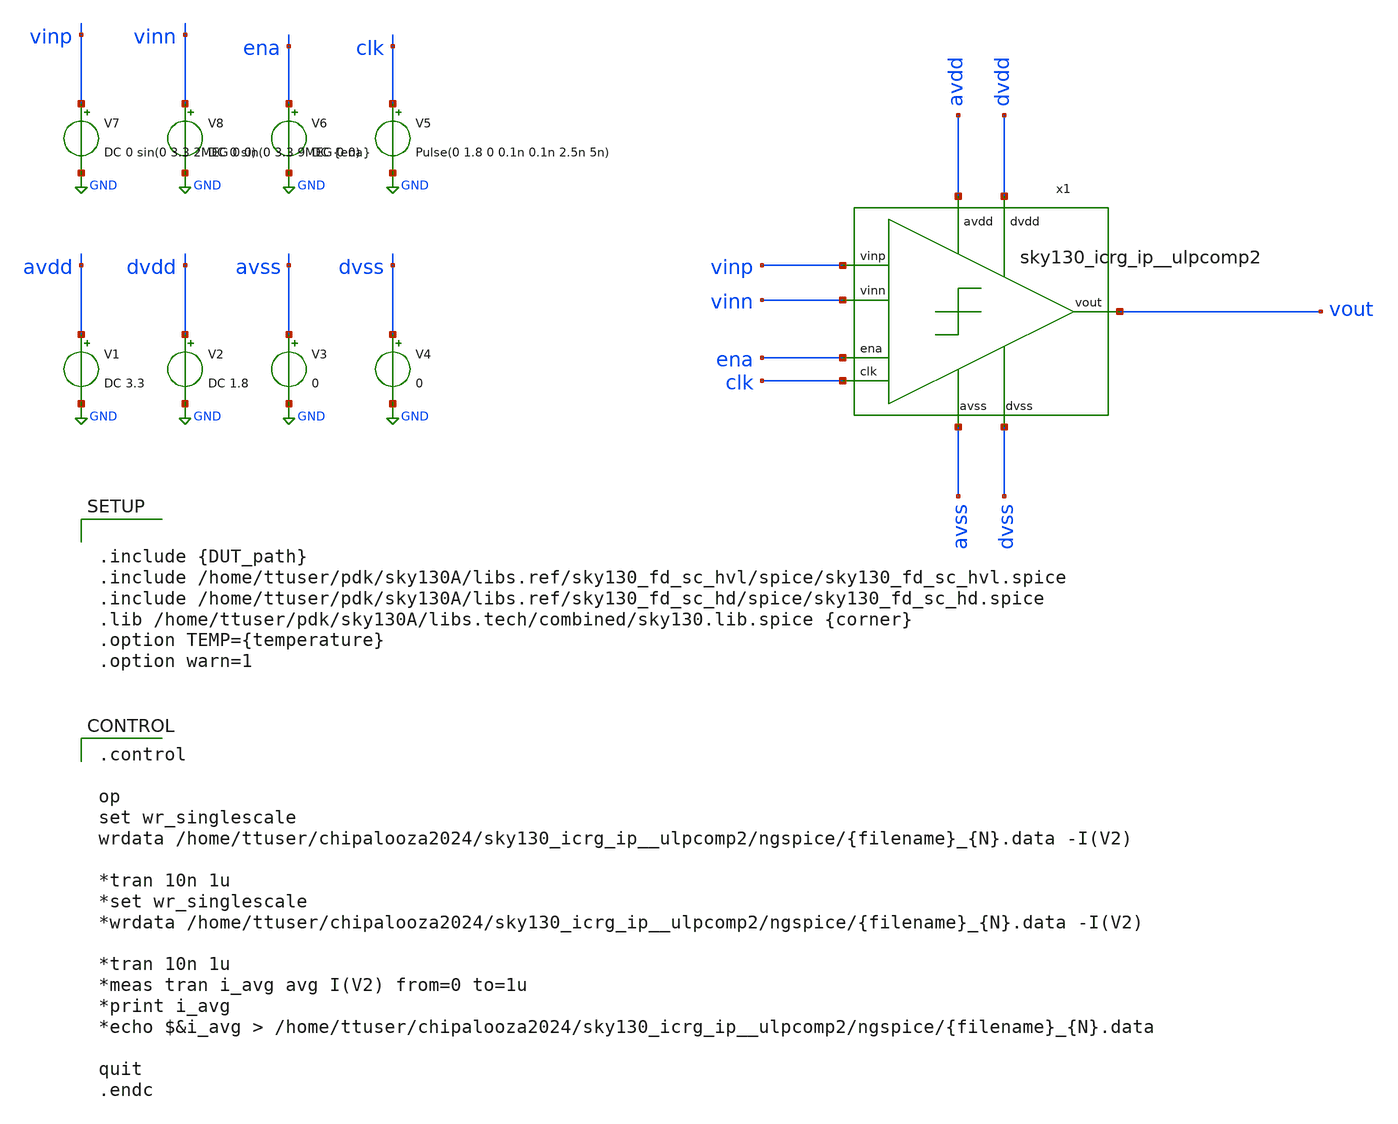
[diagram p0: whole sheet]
** sch_path: cace/current.sch
**.subckt current
x1 dvdd avdd ena vout vinn vinp clk dvss avss sky130_icrg_ip__ulpcomp2
V1 avdd GND DC 3.3
V2 dvdd GND DC 1.8
V3 avss GND 0
V4 dvss GND 0
V5 clk GND Pulse(0 1.8 0 0.1n 0.1n 2.5n 5n)
V6 ena GND DC {ena}
V7 vinp GND DC 0 sin(0 3.3 2MEG 0 0)
V8 vinn GND DC 0 sin(0 3.3 9MEG 0 0)
**** begin user architecture code


.include {DUT_path}
.include /home/ttuser/pdk/sky130A/libs.ref/sky130_fd_sc_hvl/spice/sky130_fd_sc_hvl.spice
.include /home/ttuser/pdk/sky130A/libs.ref/sky130_fd_sc_hd/spice/sky130_fd_sc_hd.spice
.lib /home/ttuser/pdk/sky130A/libs.tech/combined/sky130.lib.spice {corner}
.option TEMP={temperature}
.option warn=1


.control

op
set wr_singlescale
wrdata /home/ttuser/chipalooza2024/sky130_icrg_ip__ulpcomp2/ngspice/{filename}_{N}.data -I(V2)

*tran 10n 1u
*set wr_singlescale
*wrdata /home/ttuser/chipalooza2024/sky130_icrg_ip__ulpcomp2/ngspice/{filename}_{N}.data -I(V2)

*tran 10n 1u
*meas tran i_avg avg I(V2) from=0 to=1u
*print i_avg
*echo $&i_avg > /home/ttuser/chipalooza2024/sky130_icrg_ip__ulpcomp2/ngspice/{filename}_{N}.data

quit
.endc

**** end user architecture code
**.ends
.GLOBAL GND
.end
